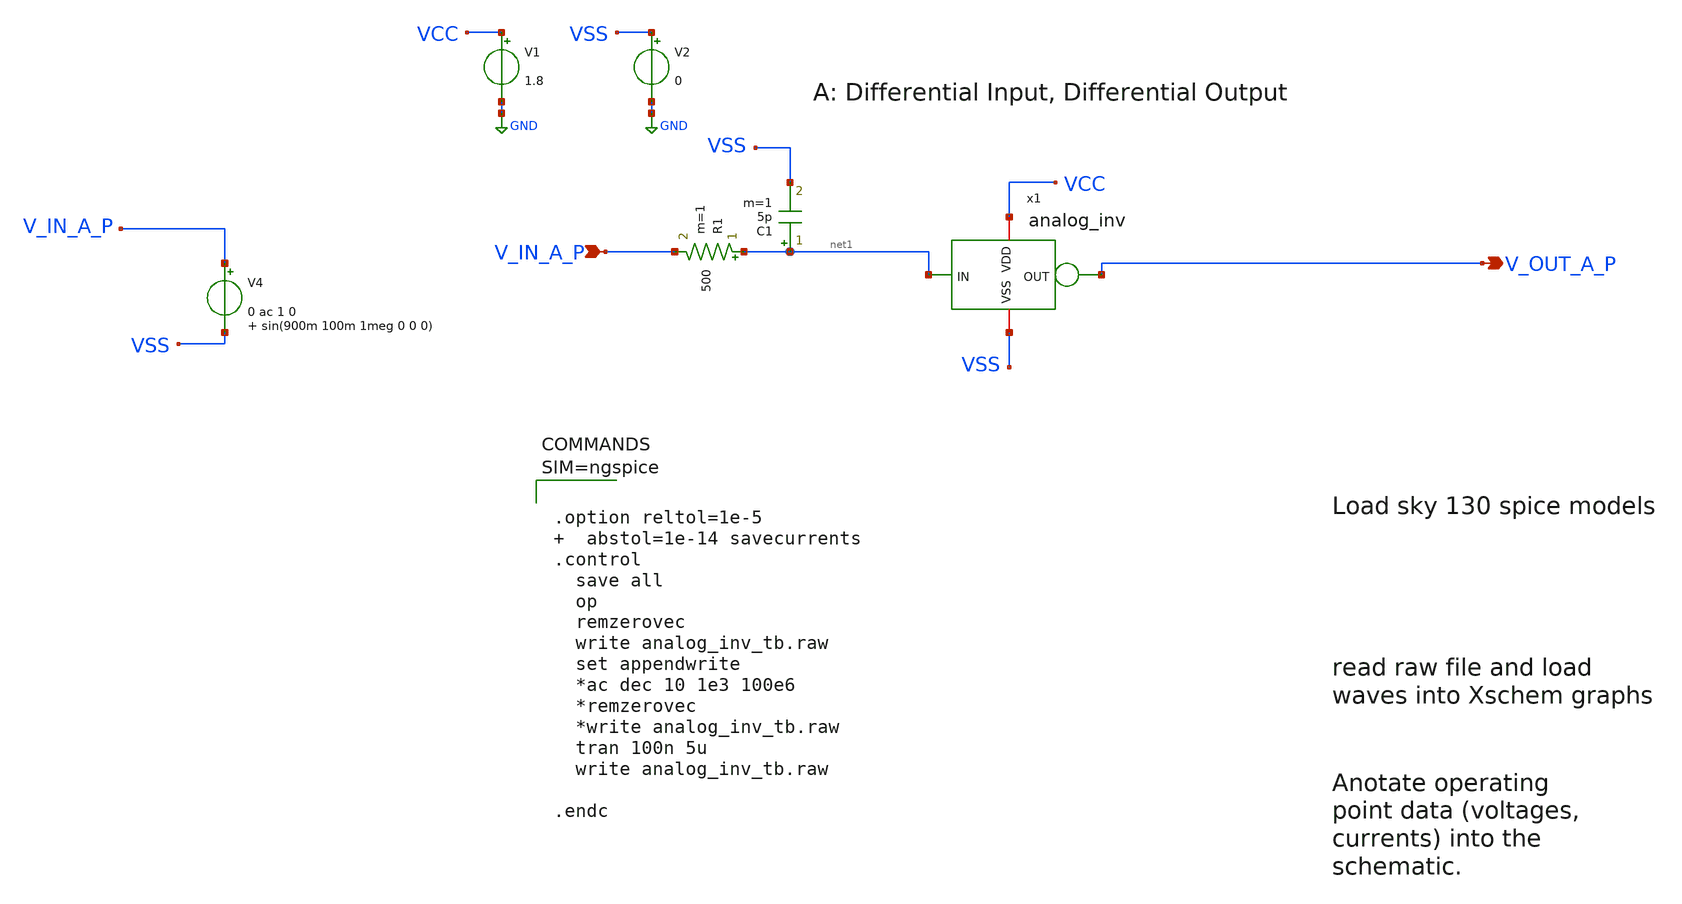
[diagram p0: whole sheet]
** sch_path: xschem/analog_inv_tb.sch
**.subckt analog_inv_tb V_IN_A_P V_OUT_A_P
*.ipin V_IN_A_P
*.opin V_OUT_A_P
V1 VCC GND 1.8
V2 VSS GND 0
V4 V_IN_A_P VSS 0 ac 1 0 sin(900m 100m 1meg 0 0 0)
R1 net1 V_IN_A_P 500 m=1
C1 net1 VSS 5p m=1
x1 VCC net1 V_OUT_A_P VSS analog_inv
**** begin user architecture code

** opencircuitdesign pdks install
.lib $::SKYWATER_MODELS/sky130.lib.spice tt





.option reltol=1e-5   abstol=1e-14 savecurrents
.control
  save all
  op
  remzerovec
  write analog_inv_tb.raw
  set appendwrite
  *ac dec 10 1e3 100e6
  *remzerovec
  *write analog_inv_tb.raw
  tran 100n 5u
  write analog_inv_tb.raw

.endc



**** end user architecture code
**.ends

* expanding   symbol:  analog_inv.sym # of pins=4
** sym_path: xschem/analog_inv.sym
** sch_path: xschem/analog_inv.sch
.subckt analog_inv VDD IN OUT VSS
*.iopin VDD
*.iopin VSS
*.ipin IN
*.opin OUT
XM2 OUT IN VSS VSS sky130_fd_pr__nfet_01v8 L=0.38 W=3.6 nf=2 ad='int((nf+1)/2) * W/nf * 0.29' as='int((nf+2)/2) * W/nf * 0.29'
+ pd='2*int((nf+1)/2) * (W/nf + 0.29)' ps='2*int((nf+2)/2) * (W/nf + 0.29)' nrd='0.29 / W' nrs='0.29 / W'
+ sa=0 sb=0 sd=0 mult=1 m=1
XM5 OUT IN VDD VDD sky130_fd_pr__pfet_01v8_lvt L=0.38 W=3.6 nf=2 ad='int((nf+1)/2) * W/nf * 0.29' as='int((nf+2)/2) * W/nf * 0.29'
+ pd='2*int((nf+1)/2) * (W/nf + 0.29)' ps='2*int((nf+2)/2) * (W/nf + 0.29)' nrd='0.29 / W' nrs='0.29 / W'
+ sa=0 sb=0 sd=0 mult=1 m=1
.ends

.GLOBAL GND
.end
